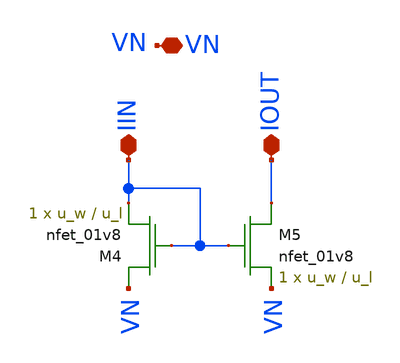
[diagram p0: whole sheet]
** sch_path: lib/analog/schematic/simple_mirror.sch
**.subckt simple_mirror VN IIN IOUT
*.iopin VN
*.iopin IIN
*.iopin IOUT
XM4 VN IIN IIN GND sky130_fd_pr__nfet_01v8 L=u_l W=u_w nf=1 ad='int((nf+1)/2) * W/nf * 0.29' as='int((nf+2)/2) * W/nf * 0.29'
+ pd='2*int((nf+1)/2) * (W/nf + 0.29)' ps='2*int((nf+2)/2) * (W/nf + 0.29)' nrd='0.29 / W' nrs='0.29 / W'
+ sa=0 sb=0 sd=0 mult=1 m=1
XM5 IOUT IIN VN GND sky130_fd_pr__nfet_01v8 L=u_l W=u_w nf=1 ad='int((nf+1)/2) * W/nf * 0.29' as='int((nf+2)/2) * W/nf * 0.29'
+ pd='2*int((nf+1)/2) * (W/nf + 0.29)' ps='2*int((nf+2)/2) * (W/nf + 0.29)' nrd='0.29 / W' nrs='0.29 / W'
+ sa=0 sb=0 sd=0 mult=1 m=1
**.ends
.end
